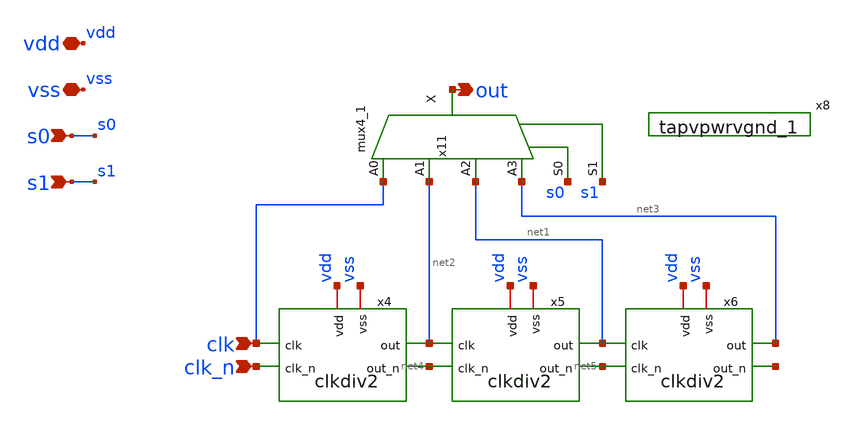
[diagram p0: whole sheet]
** sch_path: xschem/clkdiv_2n.sch
**.subckt clkdiv_2n vdd vss out s0 s1 clk clk_n
*.iopin vdd
*.iopin vss
*.opin out
*.ipin s0
*.ipin s1
*.ipin clk
*.ipin clk_n
x4 vdd vss net2 net4 clk_n clk clkdiv2
x5 vdd vss net1 net5 net4 net2 clkdiv2
x6 vdd vss net3 net6 net5 net1 clkdiv2
x11 clk net2 net1 net3 s0 s1 vss vss vdd vdd out sky130_fd_sc_hd__mux4_1
x8 vss vdd sky130_fd_sc_hd__tapvpwrvgnd_1
**.ends

* expanding   symbol:  clkdiv2.sym # of pins=6
** sym_path: xschem/clkdiv2.sym
** sch_path: xschem/clkdiv2.sch
.subckt clkdiv2 vdd vss out out_n clk_n clk
*.iopin vdd
*.opin out
*.iopin vss
*.ipin clk
*.opin out_n
*.ipin clk_n
x2 vdd vss net1 net2 out_n out clk latch
x3 vdd vss out_n out net2 net1 clk_n latch
.ends


* expanding   symbol:  latch.sym # of pins=7
** sym_path: xschem/latch.sym
** sch_path: xschem/latch.sch
.subckt latch vdd vss q_n q d d_n clk
*.iopin vdd
*.ipin d
*.opin q
*.iopin vss
*.ipin d_n
*.opin q_n
*.ipin clk
XM11 q_n q vdd vdd sky130_fd_pr__pfet_01v8 L=0.15 W=1 nf=1 ad='int((nf+1)/2) * W/nf * 0.29' as='int((nf+2)/2) * W/nf * 0.29'
+ pd='2*int((nf+1)/2) * (W/nf + 0.29)' ps='2*int((nf+2)/2) * (W/nf + 0.29)' nrd='0.29 / W' nrs='0.29 / W'
+ sa=0 sb=0 sd=0 mult=1 m=1
XM12 q q_n vdd vdd sky130_fd_pr__pfet_01v8 L=0.15 W=1 nf=1 ad='int((nf+1)/2) * W/nf * 0.29' as='int((nf+2)/2) * W/nf * 0.29'
+ pd='2*int((nf+1)/2) * (W/nf + 0.29)' ps='2*int((nf+2)/2) * (W/nf + 0.29)' nrd='0.29 / W' nrs='0.29 / W'
+ sa=0 sb=0 sd=0 mult=1 m=1
XM4 net1 clk vss vss sky130_fd_pr__nfet_01v8 L=0.15 W=2 nf=1 ad='int((nf+1)/2) * W/nf * 0.29' as='int((nf+2)/2) * W/nf * 0.29'
+ pd='2*int((nf+1)/2) * (W/nf + 0.29)' ps='2*int((nf+2)/2) * (W/nf + 0.29)' nrd='0.29 / W' nrs='0.29 / W'
+ sa=0 sb=0 sd=0 mult=1 m=1
XM1 q_n d net1 vss sky130_fd_pr__nfet_01v8 L=0.15 W=2 nf=1 ad='int((nf+1)/2) * W/nf * 0.29' as='int((nf+2)/2) * W/nf * 0.29'
+ pd='2*int((nf+1)/2) * (W/nf + 0.29)' ps='2*int((nf+2)/2) * (W/nf + 0.29)' nrd='0.29 / W' nrs='0.29 / W'
+ sa=0 sb=0 sd=0 mult=1 m=1
XM2 q d_n net1 vss sky130_fd_pr__nfet_01v8 L=0.15 W=2 nf=1 ad='int((nf+1)/2) * W/nf * 0.29' as='int((nf+2)/2) * W/nf * 0.29'
+ pd='2*int((nf+1)/2) * (W/nf + 0.29)' ps='2*int((nf+2)/2) * (W/nf + 0.29)' nrd='0.29 / W' nrs='0.29 / W'
+ sa=0 sb=0 sd=0 mult=1 m=1
.ends

.end
